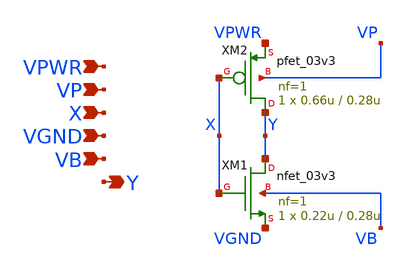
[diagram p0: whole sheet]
** sch_path: xschem/inv.sch
**.subckt inv VPWR VP X VGND VB Y
*.ipin VPWR
*.ipin VP
*.ipin X
*.ipin VGND
*.ipin VB
*.opin Y
XM1 Y X VGND VB nfet_03v3 L=0.28u W=0.22u nf=1 ad='int((nf+1)/2) * W/nf * 0.18u' as='int((nf+2)/2) * W/nf * 0.18u'
+ pd='2*int((nf+1)/2) * (W/nf + 0.18u)' ps='2*int((nf+2)/2) * (W/nf + 0.18u)' nrd='0.18u / W' nrs='0.18u / W'
+ sa=0 sb=0 sd=0 m=1
XM2 Y X VPWR VP pfet_03v3 L=0.28u W=0.66u nf=1 ad='int((nf+1)/2) * W/nf * 0.18u' as='int((nf+2)/2) * W/nf * 0.18u'
+ pd='2*int((nf+1)/2) * (W/nf + 0.18u)' ps='2*int((nf+2)/2) * (W/nf + 0.18u)' nrd='0.18u / W' nrs='0.18u / W'
+ sa=0 sb=0 sd=0 m=1
**.ends
.end
